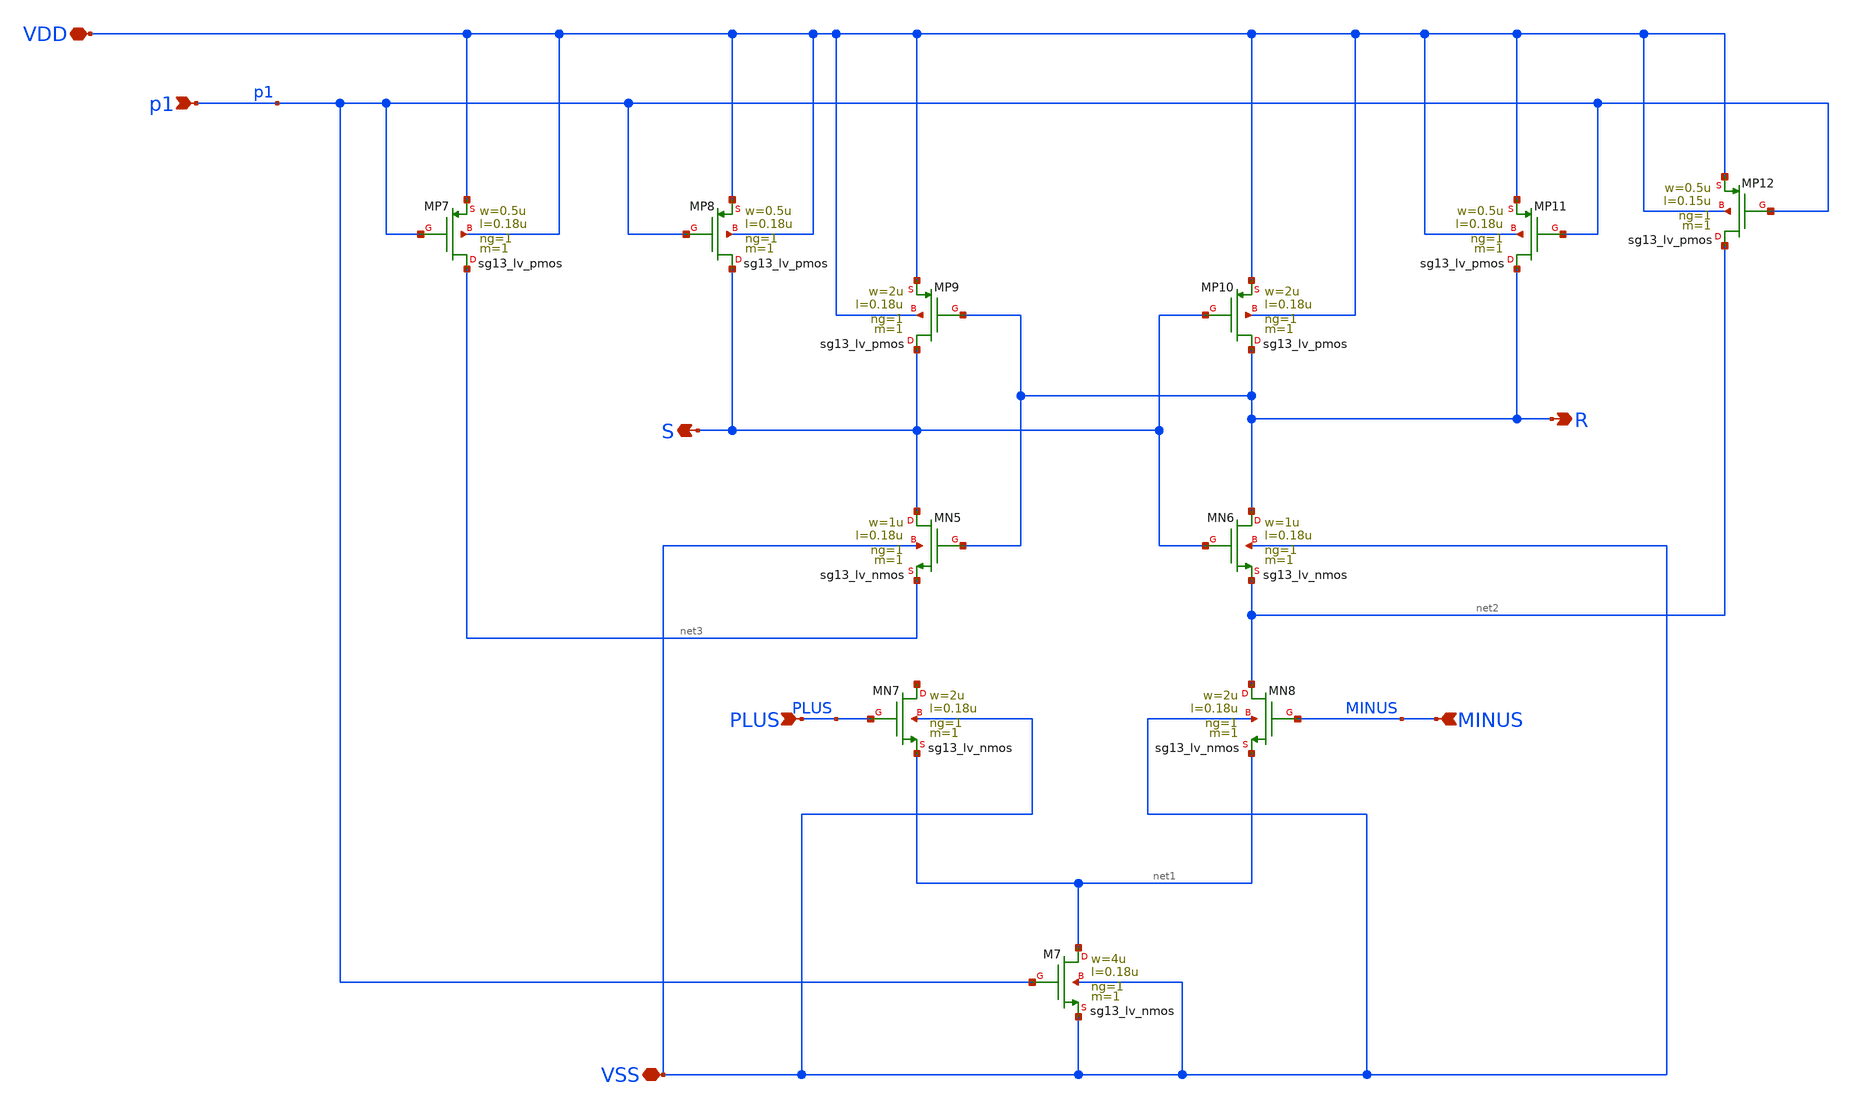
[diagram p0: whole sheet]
** sch_path: DSM/Schematics/Comparator_design_Sneha/COMPARATOR_FINAL/Comp_draft1.sch
**.subckt Comp_draft1 PLUS MINUS p1 VDD VSS R S
*.ipin PLUS
*.ipin MINUS
*.ipin p1
*.iopin VDD
*.iopin VSS
*.opin R
*.opin S
XMN5 S R net3 VSS sg13_lv_nmos w=1u l=0.18u ng=1 m=1 mm_ok=1
XMP7 net3 p1 VDD VDD sg13_lv_pmos w=0.5u l=0.18u ng=1 m=1 mm_ok=1
XMP8 S p1 VDD VDD sg13_lv_pmos w=0.5u l=0.18u ng=1 m=1 mm_ok=1
XMP9 S R VDD VDD sg13_lv_pmos w=2u l=0.18u ng=1 m=1 mm_ok=1
XMP10 R S VDD VDD sg13_lv_pmos w=2u l=0.18u ng=1 m=1 mm_ok=1
XMP11 R p1 VDD VDD sg13_lv_pmos w=0.5u l=0.18u ng=1 m=1 mm_ok=1
XMP12 net2 p1 VDD VDD sg13_lv_pmos w=0.5u l=0.15u ng=1 m=1 mm_ok=1
XMN6 R S net2 VSS sg13_lv_nmos w=1u l=0.18u ng=1 m=1 mm_ok=1
XMN7 net4 PLUS net1 VSS sg13_lv_nmos w=2u l=0.18u ng=1 m=1 mm_ok=1
XMN8 net2 MINUS net1 VSS sg13_lv_nmos w=2u l=0.18u ng=1 m=1 mm_ok=1
XM7 net1 p1 VSS VSS sg13_lv_nmos w=4u l=0.18u ng=1 m=1 mm_ok=1
**** begin user architecture code
 .lib $::SG13G2_MODELS/cornerMOSlv.lib mos_tt
.lib $::SG13G2_MODELS/cornerCAP.lib cap_typ
.inc $::PDK_ROOT/ihp-sg13g2/libs.ref/sg13g2_stdcell/spice/sg13g2_stdcell.spice

**** end user architecture code
**.ends
.end
